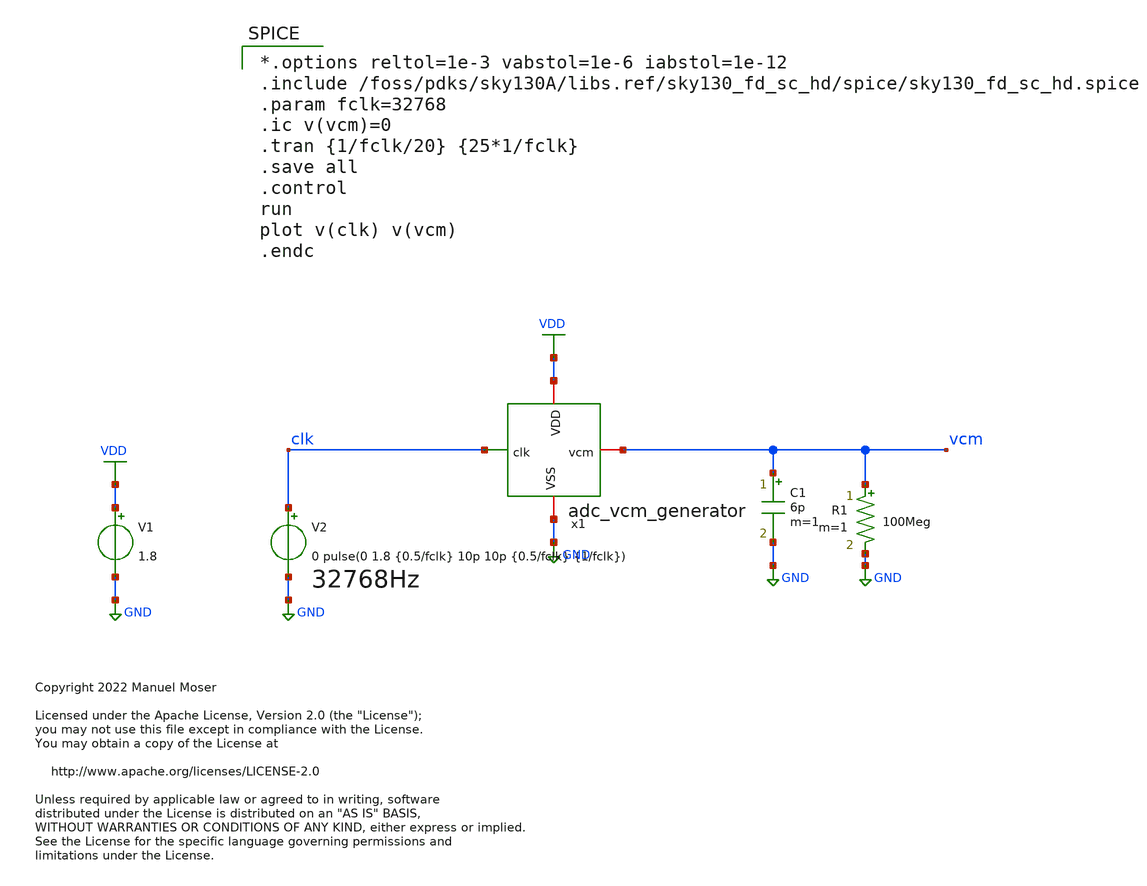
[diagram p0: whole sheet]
** sch_path: hgu/tb/adc_vcm_generator_tb.sch
* Copyright 2022 Manuel Moser
* Licensed under the Apache License, Version 2.0 (the "License");
**.subckt adc_vcm_generator_tb
V1 VDD GND 1.8
V2 clk GND 0 pulse(0 1.8 {0.5/fclk} 10p 10p {0.5/fclk} {1/fclk})
C1 vcm GND 6p m=1
R1 vcm GND 100Meg m=1
x1 VDD vcm clk GND adc_vcm_generator
**** begin user architecture code

*.options reltol=1e-3 vabstol=1e-6 iabstol=1e-12
.include /foss/pdks/sky130A/libs.ref/sky130_fd_sc_hd/spice/sky130_fd_sc_hd.spice
.param fclk=32768
.ic v(vcm)=0
.tran {1/fclk/20} {25*1/fclk}
.save all
.control
run
plot v(clk) v(vcm)
.endc



** opencircuitdesign pdks install
.lib $::SKYWATER_MODELS/sky130.lib.spice tt


**** end user architecture code
**.ends
.GLOBAL GND
.GLOBAL VDD
.end
